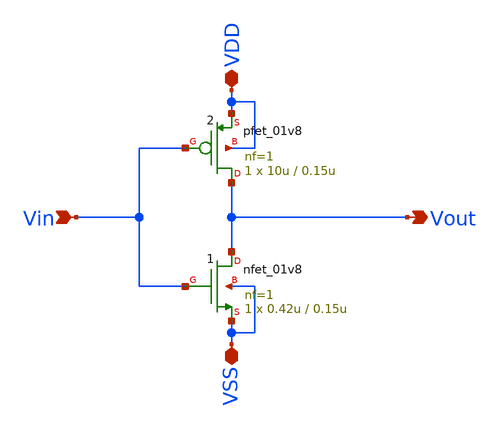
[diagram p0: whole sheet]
** sch_path: actual-layout/layout_design.sch
**.subckt layout_design VDD Vin VSS Vout
*.iopin VDD
*.ipin Vin
*.iopin VSS
*.opin Vout
X1 Vout Vin VSS VSS sky130_fd_pr__nfet_01v8 L=0.15u W=0.42u nf=1 ad='int((1 + 1)/2) * 0.42u / 1 * 0.29'
+ as='int((1 + 2)/2) * 0.42u / 1 * 0.29' pd='2*int((1 + 1)/2) * (0.42u / 1 + 0.29)' ps='2*int((1 + 2)/2) * (0.42u / 1 + 0.29)'
+ nrd='0.29 / 0.42u ' nrs='0.29 / 0.42u ' sa=0 sb=0 sd=0 mult=1 m=1
X2 Vout Vin VDD VDD sky130_fd_pr__pfet_01v8 L=0.15u W=10u nf=1 ad='int((1 + 1)/2) * 10u / 1 * 0.29' as='int((1 + 2)/2) * 10u / 1 * 0.29'
+ pd='2*int((1 + 1)/2) * (10u / 1 + 0.29)' ps='2*int((1 + 2)/2) * (10u / 1 + 0.29)' nrd='0.29 / 10u ' nrs='0.29 / 10u '
+ sa=0 sb=0 sd=0 mult=1 m=1
**.ends
.end
